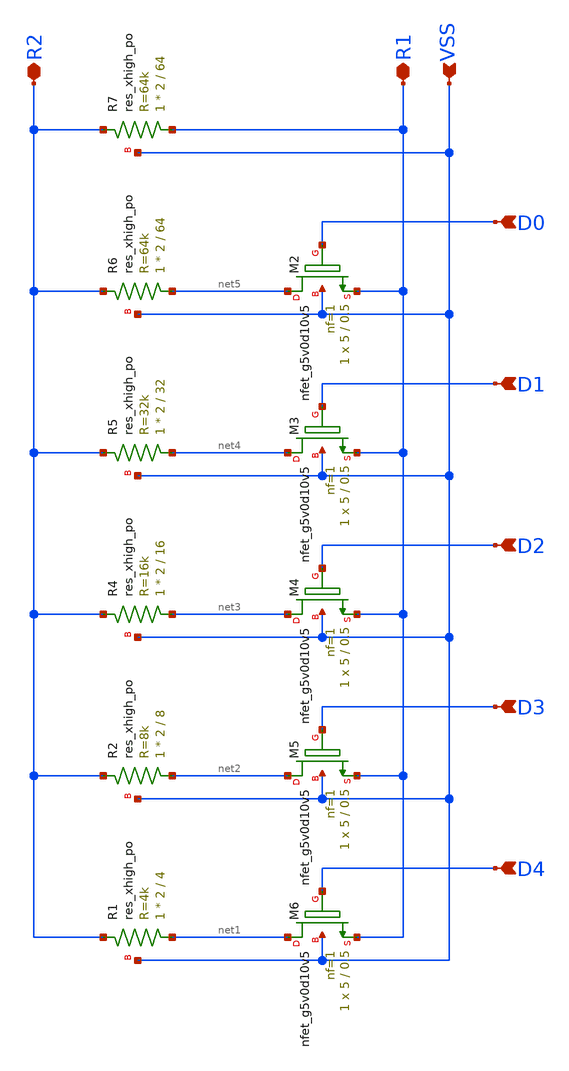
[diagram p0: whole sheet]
** sch_path: xschem/RA_array.sch
**.subckt RA_array VSS R2 D0 D1 D2 D3 D4 R1
*.ipin VSS
*.iopin R2
*.ipin D0
*.ipin D1
*.ipin D2
*.ipin D3
*.ipin D4
*.iopin R1
XR1 net1 R2 VSS sky130_fd_pr__res_xhigh_po W=2 L=4 mult=1 m=1
XR4 net3 R2 VSS sky130_fd_pr__res_xhigh_po W=2 L=16 mult=1 m=1
XR5 net4 R2 VSS sky130_fd_pr__res_xhigh_po W=2 L=32 mult=1 m=1
XR6 net5 R2 VSS sky130_fd_pr__res_xhigh_po W=2 L=64 mult=1 m=1
XR7 R1 R2 VSS sky130_fd_pr__res_xhigh_po W=2 L=64 mult=1 m=1
XM2 net5 D0 R1 VSS sky130_fd_pr__nfet_g5v0d10v5 L=0.5 W=5 nf=1 ad='int((nf+1)/2) * W/nf * 0.29' as='int((nf+2)/2) * W/nf * 0.29'
+ pd='2*int((nf+1)/2) * (W/nf + 0.29)' ps='2*int((nf+2)/2) * (W/nf + 0.29)' nrd='0.29 / W' nrs='0.29 / W'
+ sa=0 sb=0 sd=0 mult=1 m=1
XM3 net4 D1 R1 VSS sky130_fd_pr__nfet_g5v0d10v5 L=0.5 W=5 nf=1 ad='int((nf+1)/2) * W/nf * 0.29' as='int((nf+2)/2) * W/nf * 0.29'
+ pd='2*int((nf+1)/2) * (W/nf + 0.29)' ps='2*int((nf+2)/2) * (W/nf + 0.29)' nrd='0.29 / W' nrs='0.29 / W'
+ sa=0 sb=0 sd=0 mult=1 m=1
XM4 net3 D2 R1 VSS sky130_fd_pr__nfet_g5v0d10v5 L=0.5 W=5 nf=1 ad='int((nf+1)/2) * W/nf * 0.29' as='int((nf+2)/2) * W/nf * 0.29'
+ pd='2*int((nf+1)/2) * (W/nf + 0.29)' ps='2*int((nf+2)/2) * (W/nf + 0.29)' nrd='0.29 / W' nrs='0.29 / W'
+ sa=0 sb=0 sd=0 mult=1 m=1
XM5 net2 D3 R1 VSS sky130_fd_pr__nfet_g5v0d10v5 L=0.5 W=5 nf=1 ad='int((nf+1)/2) * W/nf * 0.29' as='int((nf+2)/2) * W/nf * 0.29'
+ pd='2*int((nf+1)/2) * (W/nf + 0.29)' ps='2*int((nf+2)/2) * (W/nf + 0.29)' nrd='0.29 / W' nrs='0.29 / W'
+ sa=0 sb=0 sd=0 mult=1 m=1
XM6 net1 D4 R1 VSS sky130_fd_pr__nfet_g5v0d10v5 L=0.5 W=5 nf=1 ad='int((nf+1)/2) * W/nf * 0.29' as='int((nf+2)/2) * W/nf * 0.29'
+ pd='2*int((nf+1)/2) * (W/nf + 0.29)' ps='2*int((nf+2)/2) * (W/nf + 0.29)' nrd='0.29 / W' nrs='0.29 / W'
+ sa=0 sb=0 sd=0 mult=1 m=1
XR2 net2 R2 VSS sky130_fd_pr__res_xhigh_po W=2 L=8 mult=1 m=1
**.ends
.end
